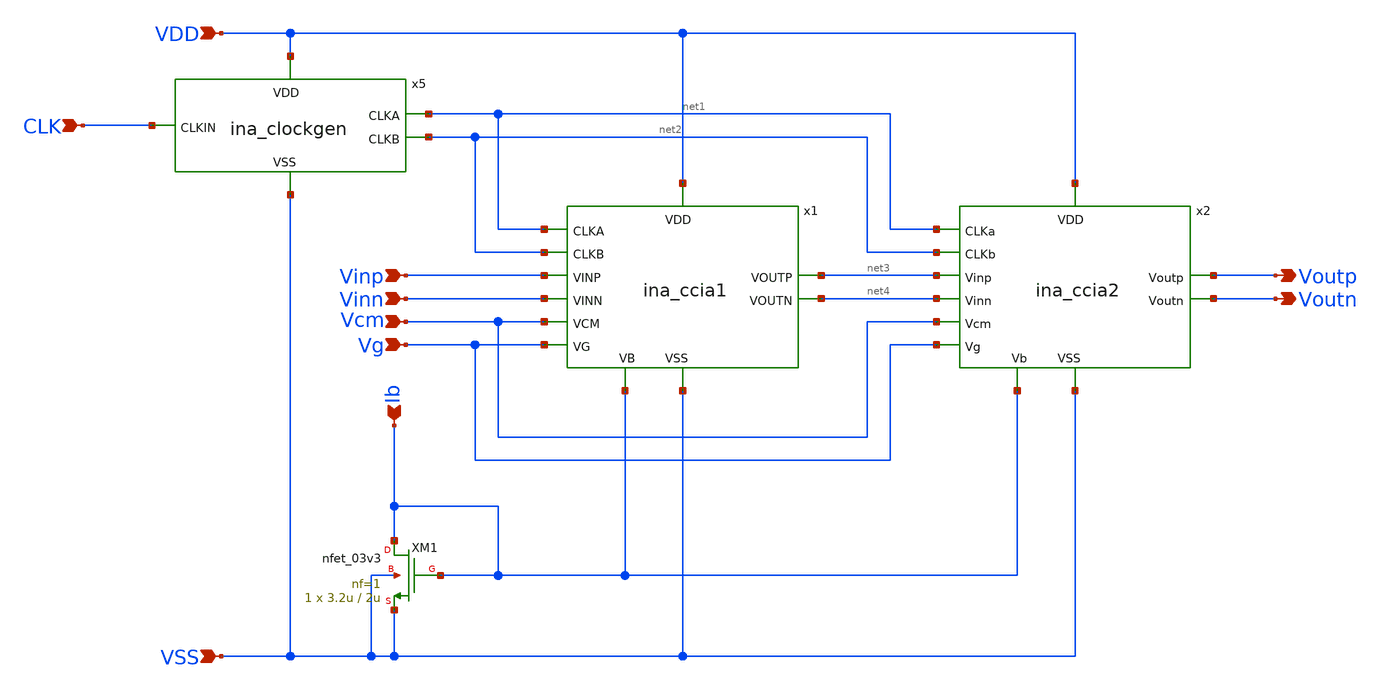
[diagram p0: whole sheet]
** sch_path: designs/libs/core_ina/ina/ina.sch
**.subckt ina CLK Vinp Vinn VDD VSS Vcm Ib Vg Voutp Voutn
*.ipin CLK
*.ipin Vinp
*.ipin Vinn
*.ipin VDD
*.ipin VSS
*.ipin Vcm
*.ipin Ib
*.ipin Vg
*.opin Voutp
*.opin Voutn
x5 VDD CLK net1 net2 VSS ina_clockgen
XM1 Ib Ib VSS VSS nfet_03v3 L=2u W=3.2u nf=1 ad='int((nf+1)/2) * W/nf * 0.18u' as='int((nf+2)/2) * W/nf * 0.18u'
+ pd='2*int((nf+1)/2) * (W/nf + 0.18u)' ps='2*int((nf+2)/2) * (W/nf + 0.18u)' nrd='0.18u / W' nrs='0.18u / W'
+ sa=0 sb=0 sd=0 m=1
x1 Vg Vinp VDD net3 Vinn net4 net1 net2 Vcm Ib VSS ina_ccia1
x2 Vg net3 VDD Voutp net4 Voutn net1 net2 Vcm Ib VSS ina_ccia2
**.ends
.end
